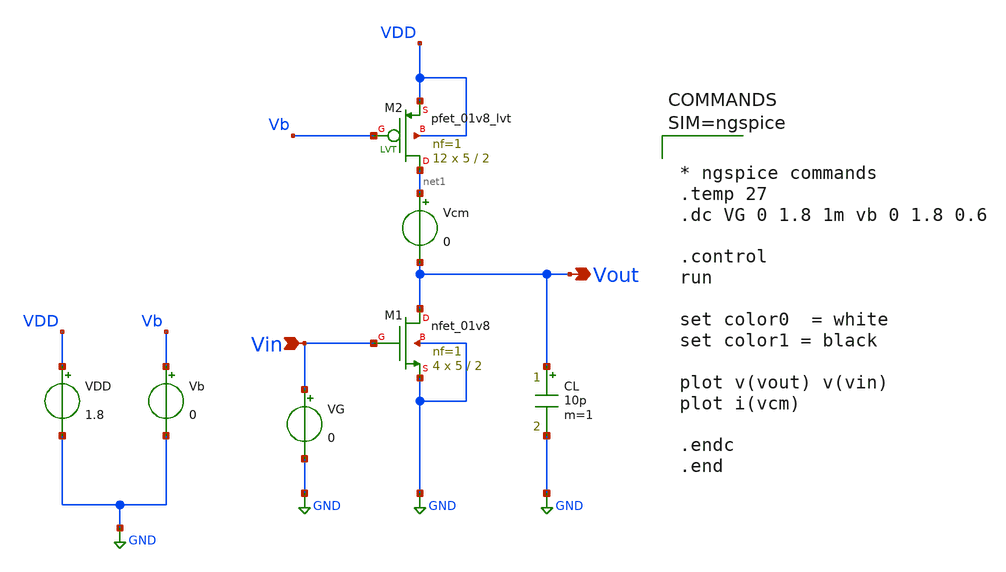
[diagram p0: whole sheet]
** sch_path: Common_Source_PMOS_Load_ckts/CS_Amp_PMOS_Triode_Load_Ckts/CS_Amp_PMOS_Triode_Load_DC_Analysis.sch
**.subckt CS_Amp_PMOS_Triode_Load_DC_Analysis Vin Vout
*.ipin Vin
*.opin Vout
XM1 Vout Vin GND GND sky130_fd_pr__nfet_01v8 L=2 W=5 nf=1 ad='int((1 + 1)/2) * 5 / 1 * 0.29' as='int((1 + 2)/2) * 5 / 1 * 0.29'
+ pd='2*int((1 + 1)/2) * (5 / 1 + 0.29)' ps='2*int((1 + 2)/2) * (5 / 1 + 0.29)' nrd='0.29 / 5 ' nrs='0.29 / 5 '
+ sa=0 sb=0 sd=0 mult=4 m=4
XM2 net1 Vb VDD VDD sky130_fd_pr__pfet_01v8_lvt L=2 W=5 nf=1 ad='int((1 + 1)/2) * 5 / 1 * 0.29' as='int((1 + 2)/2) * 5 / 1 * 0.29'
+ pd='2*int((1 + 1)/2) * (5 / 1 + 0.29)' ps='2*int((1 + 2)/2) * (5 / 1 + 0.29)' nrd='0.29 / 5 ' nrs='0.29 / 5 '
+ sa=0 sb=0 sd=0 mult=12 m=12
Vcm net1 Vout 0
VG Vin GND 0
Vb Vb GND 0
VDD VDD GND 1.8
CL Vout GND 10p m=1
**** begin user architecture code



* ngspice commands
.temp 27
.dc VG 0 1.8 1m vb 0 1.8 0.6

.control
run

set color0  = white
set color1 = black

plot v(vout) v(vin)
plot i(vcm)

.endc
.end





** opencircuitdesign pdks install
.lib $::SKYWATER_MODELS/sky130.lib.spice tt

**** end user architecture code
**.ends
.GLOBAL GND
.end
